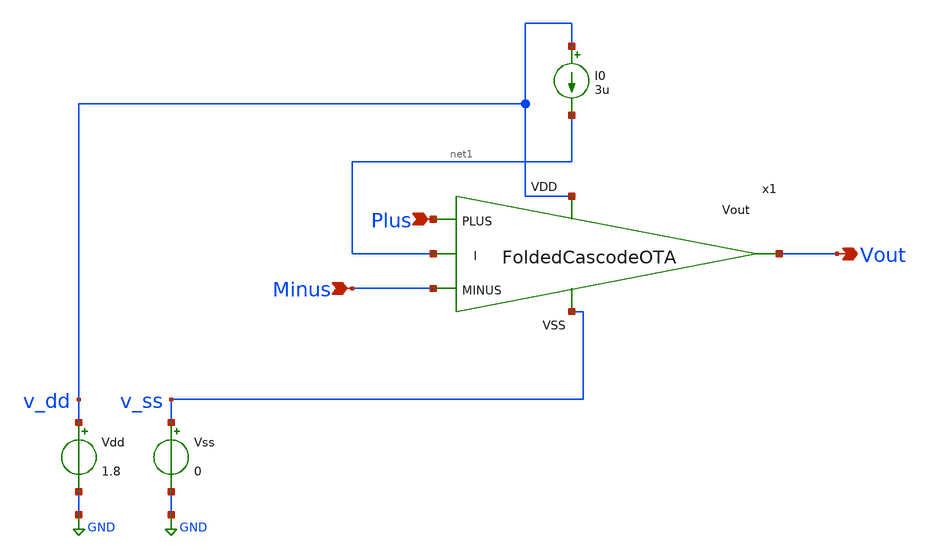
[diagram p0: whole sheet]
** sch_path: DSM/Schematics/IC_Designs_Hrishi/RealCircuits/VCCS_FolCas.sch
* DSM/Schematics/IC_Designs_Hrishi/RealCircuits/Folded Cascode/FoldedCascodeOTA.sch:
* (c) 2024 Hrishikesh, @HSB
**.subckt VCCS_FolCas Minus Vout Plus
*.ipin Minus
*.opin Vout
*.ipin Plus
Vdd v_dd GND 1.8
Vss v_ss GND 0
I0 v_dd net1 3u
x1 v_dd net1 Plus Minus Vout v_ss FoldedCascodeOTA
**.ends

* expanding   symbol:  /foss/designs/CEMS_DSM/DSM/Schematics/IC_Designs_Hrishi/RealCircuits/Folded
*+ Cascode/FoldedCascodeOTA.sym # of pins=6
** sym_path: DSM/Schematics/IC_Designs_Hrishi/RealCircuits/Folded Cascode/FoldedCascodeOTA.sym
** sch_path: DSM/Schematics/IC_Designs_Hrishi/RealCircuits/Folded Cascode/FoldedCascodeOTA.sch
.subckt FoldedCascodeOTA VDD I PLUS MINUS Vout VSS
*.ipin PLUS
*.ipin MINUS
*.opin Vout
*.ipin VDD
*.ipin VSS
*.ipin I
XM1 net2 net4 VDD VDD sg13_lv_pmos w=0.272u l=0.5u ng=1 m=1 mm_ok=1
XM2 net1 PLUS net2 VDD sg13_lv_pmos w=0.136u l=0.5u ng=1 m=1 mm_ok=1
XM3 net6 MINUS net2 VDD sg13_lv_pmos w=0.136u l=0.5u ng=1 m=1 mm_ok=1
XM14 net6 net9 VSS VSS sg13_lv_nmos w=0.30u l=2u ng=1 m=1 mm_ok=1
XM13 Vout I net6 VSS sg13_lv_nmos w=0.15u l=2u ng=1 m=1 mm_ok=1
XM11 net7 I net1 VSS sg13_lv_nmos w=0.15u l=2u ng=1 m=1 mm_ok=1
XM12 net1 net9 VSS VSS sg13_lv_nmos w=0.30u l=2u ng=1 m=1 mm_ok=1
XM5 Vout net3 net5 VDD sg13_lv_pmos w=0.136u l=0.5u ng=1 m=1 mm_ok=1
XM4 net5 net4 VDD VDD sg13_lv_pmos w=0.136u l=0.5u ng=1 m=1 mm_ok=1
XM6 net4 net4 VDD VDD sg13_lv_pmos w=0.136u l=0.5u ng=1 m=1 mm_ok=1
XM8 net3 net3 net4 VDD sg13_lv_pmos w=0.136u l=0.5u ng=1 m=1 mm_ok=1
XM9 net8 net4 VDD VDD sg13_lv_pmos w=0.136u l=0.5u ng=1 m=1 mm_ok=1
XM10 net7 net3 net8 VDD sg13_lv_pmos w=0.136u l=0.5u ng=1 m=1 mm_ok=1
XM16 I I net9 VSS sg13_lv_nmos w=0.15u l=2u ng=1 m=1 mm_ok=1
XM15 net9 net9 VSS VSS sg13_lv_nmos w=0.15u l=2u ng=1 m=1 mm_ok=1
XM7 net3 net9 VSS VSS sg13_lv_nmos w=0.15u l=2u ng=1 m=1 mm_ok=1
XM18 VDD I net10 VSS sg13_lv_nmos w=0.15u l=2u ng=1 m=1 mm_ok=1
XM17 net10 net9 VSS VSS sg13_lv_nmos w=0.15u l=2u ng=1 m=1 mm_ok=1
.ends

.GLOBAL GND
.end
